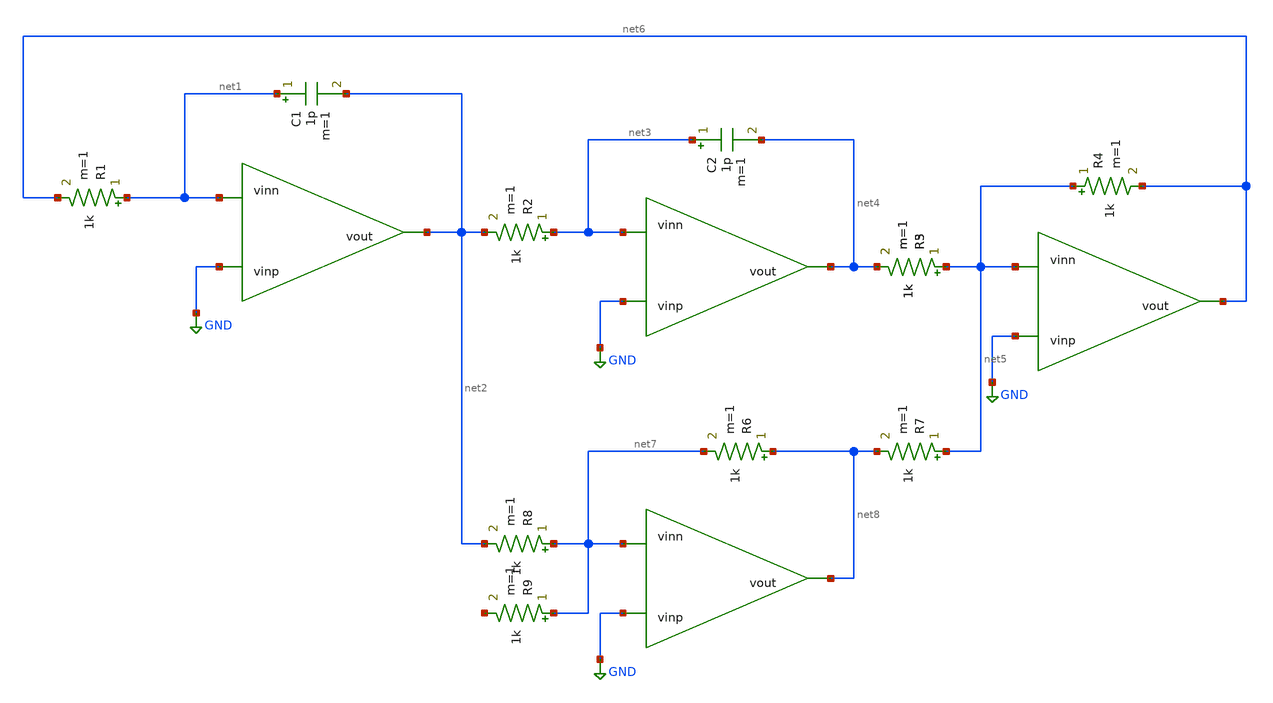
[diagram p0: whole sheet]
** sch_path: 2_Ideal_Cir/toplevel.sch
**.subckt toplevel
R1 net1 net6 1k m=1
C1 net1 net2 1p m=1
R2 net3 net2 1k m=1
C2 net3 net4 1p m=1
R3 net5 net4 1k m=1
R4 net5 net6 1k m=1
R5 net5 net4 1k m=1
R6 net8 net7 1k m=1
R7 net5 net8 1k m=1
R8 net7 net2 1k m=1
R9 net7 net9 1k m=1
**.ends
.GLOBAL GND
.end
